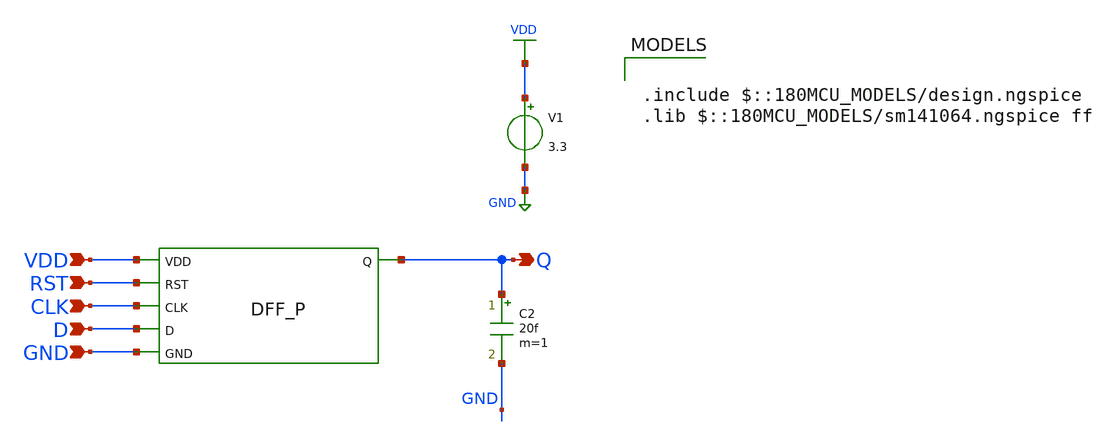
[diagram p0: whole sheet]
** sch_path: blocks/adc/encoder/tb/dff_postlayout_tb.sch
**.subckt dff_postlayout_tb Q D VDD GND RST CLK
*.opin Q
*.ipin D
*.ipin VDD
*.ipin GND
*.ipin RST
*.ipin CLK
C2 Q GND 20f m=1
x1 VDD RST CLK D Q GND dff_encoder
V1 VDD GND 3.3
**** begin user architecture code

.include $::180MCU_MODELS/design.ngspice
.lib $::180MCU_MODELS/sm141064.ngspice ff



.include /foss/designs/encoder/layout/dff/dff_encoder_sim.spice

V_CLK CLK 0 pulse(0 3.3 260p 10p 10p 290p 500p)
V_D D 0 pwl(0 0 150p 0 160p 3.3 400p 3.3 410p 0 1100p 0 1110p 3.3 1400p 3.3 1410p 0 2100p 0 2110p
+ 3.3 2400p 3.3 2410p 0 3100p 0 3110p 3.3 3400p 3.3 3410p 0 4100p 0 4110p 3.3 4400p 3.3 4410p 0 5n 0))
V_RST RST 0 pulse(0 3.3 150p 10p 10p 5n 10n)
.control

  save CLK D RST Q
  run
  write tspc_dff_layout_test.raw
.endc
.tran 1p 5n


**** end user architecture code
**.ends
.GLOBAL VDD
.GLOBAL GND
.end
